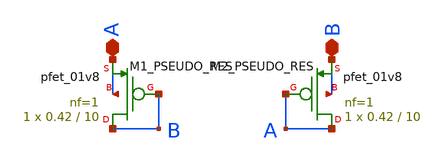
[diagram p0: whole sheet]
** sch_path: xschem/pseudo_res.sch
**.subckt pseudo_res A B
*.iopin A
*.iopin B
XM1_PSEUDO_RES B B A A sky130_fd_pr__pfet_01v8 L=10 W=0.42 nf=1 ad='int((1 + 1)/2) * 0.42 / 1 * 0.29'
+ as='int((1 + 2)/2) * 0.42 / 1 * 0.29' pd='2*int((1 + 1)/2) * (0.42 / 1 + 0.29)' ps='2*int((1 + 2)/2) * (0.42 / 1 + 0.29)'
+ nrd='0.29 / 0.42 ' nrs='0.29 / 0.42 ' sa=0 sb=0 sd=0 mult=1 m=1
XM2_PSEUDO_RES A A B B sky130_fd_pr__pfet_01v8 L=10 W=0.42 nf=1 ad='int((1 + 1)/2) * 0.42 / 1 * 0.29'
+ as='int((1 + 2)/2) * 0.42 / 1 * 0.29' pd='2*int((1 + 1)/2) * (0.42 / 1 + 0.29)' ps='2*int((1 + 2)/2) * (0.42 / 1 + 0.29)'
+ nrd='0.29 / 0.42 ' nrs='0.29 / 0.42 ' sa=0 sb=0 sd=0 mult=1 m=1
**.ends
.end
